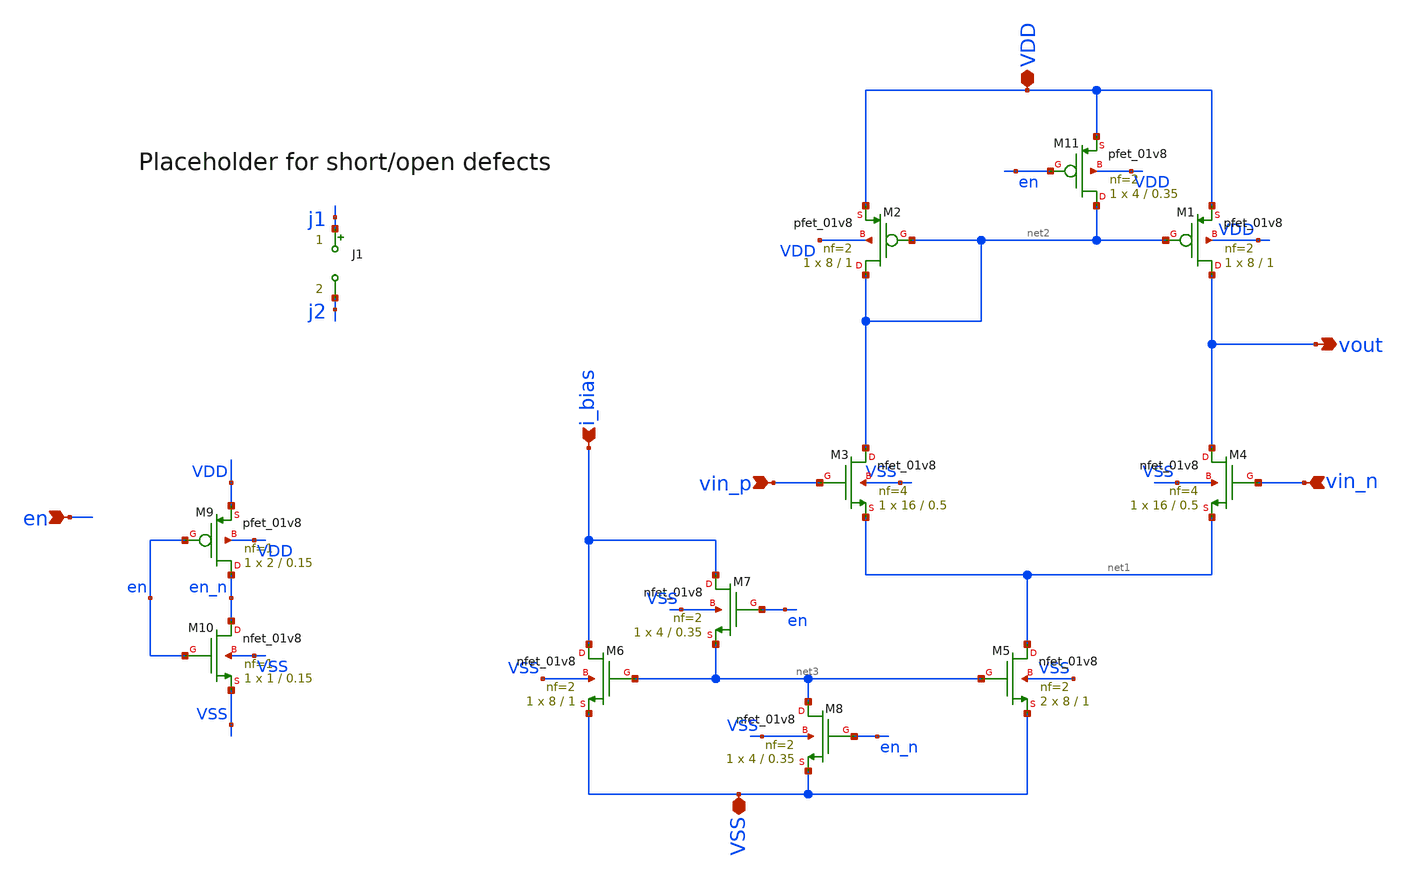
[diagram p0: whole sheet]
** sch_path: ISSCC_2025_V1/xschem/Benchmark_Circuits/OpAmp/OpAmp.sch
**.subckt OpAmp vin_p vin_n VSS VDD vout i_bias en
*.ipin vin_p
*.ipin vin_n
*.iopin VSS
*.iopin VDD
*.opin vout
*.ipin i_bias
*.ipin en
XM1 vout net2 VDD VDD sky130_fd_pr__pfet_01v8 L=1 W=8 nf=2 ad='int((nf+1)/2) * W/nf * 0.29' as='int((nf+2)/2) * W/nf * 0.29'
+ pd='2*int((nf+1)/2) * (W/nf + 0.29)' ps='2*int((nf+2)/2) * (W/nf + 0.29)' nrd='0.29 / W' nrs='0.29 / W'
+ sa=0 sb=0 sd=0 mult=1 m=1
XM2 net2 net2 VDD VDD sky130_fd_pr__pfet_01v8 L=1 W=8 nf=2 ad='int((nf+1)/2) * W/nf * 0.29' as='int((nf+2)/2) * W/nf * 0.29'
+ pd='2*int((nf+1)/2) * (W/nf + 0.29)' ps='2*int((nf+2)/2) * (W/nf + 0.29)' nrd='0.29 / W' nrs='0.29 / W'
+ sa=0 sb=0 sd=0 mult=1 m=1
XM3 net2 vin_p net1 VSS sky130_fd_pr__nfet_01v8 L=0.5 W=16 nf=4 ad='int((nf+1)/2) * W/nf * 0.29' as='int((nf+2)/2) * W/nf * 0.29'
+ pd='2*int((nf+1)/2) * (W/nf + 0.29)' ps='2*int((nf+2)/2) * (W/nf + 0.29)' nrd='0.29 / W' nrs='0.29 / W'
+ sa=0 sb=0 sd=0 mult=1 m=1
XM4 vout vin_n net1 VSS sky130_fd_pr__nfet_01v8 L=0.5 W=16 nf=4 ad='int((nf+1)/2) * W/nf * 0.29' as='int((nf+2)/2) * W/nf * 0.29'
+ pd='2*int((nf+1)/2) * (W/nf + 0.29)' ps='2*int((nf+2)/2) * (W/nf + 0.29)' nrd='0.29 / W' nrs='0.29 / W'
+ sa=0 sb=0 sd=0 mult=1 m=1
XM5 net1 net3 VSS VSS sky130_fd_pr__nfet_01v8 L=1 W=8 nf=2 ad='int((nf+1)/2) * W/nf * 0.29' as='int((nf+2)/2) * W/nf * 0.29'
+ pd='2*int((nf+1)/2) * (W/nf + 0.29)' ps='2*int((nf+2)/2) * (W/nf + 0.29)' nrd='0.29 / W' nrs='0.29 / W'
+ sa=0 sb=0 sd=0 mult=2 m=2
XM6 i_bias net3 VSS VSS sky130_fd_pr__nfet_01v8 L=1 W=8 nf=2 ad='int((nf+1)/2) * W/nf * 0.29' as='int((nf+2)/2) * W/nf * 0.29'
+ pd='2*int((nf+1)/2) * (W/nf + 0.29)' ps='2*int((nf+2)/2) * (W/nf + 0.29)' nrd='0.29 / W' nrs='0.29 / W'
+ sa=0 sb=0 sd=0 mult=1 m=1
XM9 en_n en VDD VDD sky130_fd_pr__pfet_01v8 L=0.15 W=2 nf=1 ad='int((nf+1)/2) * W/nf * 0.29' as='int((nf+2)/2) * W/nf * 0.29'
+ pd='2*int((nf+1)/2) * (W/nf + 0.29)' ps='2*int((nf+2)/2) * (W/nf + 0.29)' nrd='0.29 / W' nrs='0.29 / W'
+ sa=0 sb=0 sd=0 mult=1 m=1
XM10 en_n en VSS VSS sky130_fd_pr__nfet_01v8 L=0.15 W=1 nf=1 ad='int((nf+1)/2) * W/nf * 0.29' as='int((nf+2)/2) * W/nf * 0.29'
+ pd='2*int((nf+1)/2) * (W/nf + 0.29)' ps='2*int((nf+2)/2) * (W/nf + 0.29)' nrd='0.29 / W' nrs='0.29 / W'
+ sa=0 sb=0 sd=0 mult=1 m=1
XM7 i_bias en net3 VSS sky130_fd_pr__nfet_01v8 L=0.35 W=4 nf=2 ad='int((nf+1)/2) * W/nf * 0.29' as='int((nf+2)/2) * W/nf * 0.29'
+ pd='2*int((nf+1)/2) * (W/nf + 0.29)' ps='2*int((nf+2)/2) * (W/nf + 0.29)' nrd='0.29 / W' nrs='0.29 / W'
+ sa=0 sb=0 sd=0 mult=1 m=1
XM8 net3 en_n VSS VSS sky130_fd_pr__nfet_01v8 L=0.35 W=4 nf=2 ad='int((nf+1)/2) * W/nf * 0.29' as='int((nf+2)/2) * W/nf * 0.29'
+ pd='2*int((nf+1)/2) * (W/nf + 0.29)' ps='2*int((nf+2)/2) * (W/nf + 0.29)' nrd='0.29 / W' nrs='0.29 / W'
+ sa=0 sb=0 sd=0 mult=1 m=1
XM11 net2 en VDD VDD sky130_fd_pr__pfet_01v8 L=0.35 W=4 nf=2 ad='int((nf+1)/2) * W/nf * 0.29' as='int((nf+2)/2) * W/nf * 0.29'
+ pd='2*int((nf+1)/2) * (W/nf + 0.29)' ps='2*int((nf+2)/2) * (W/nf + 0.29)' nrd='0.29 / W' nrs='0.29 / W'
+ sa=0 sb=0 sd=0 mult=1 m=1
* J1 ?1 j1 ?1 j2
**.ends
.end
